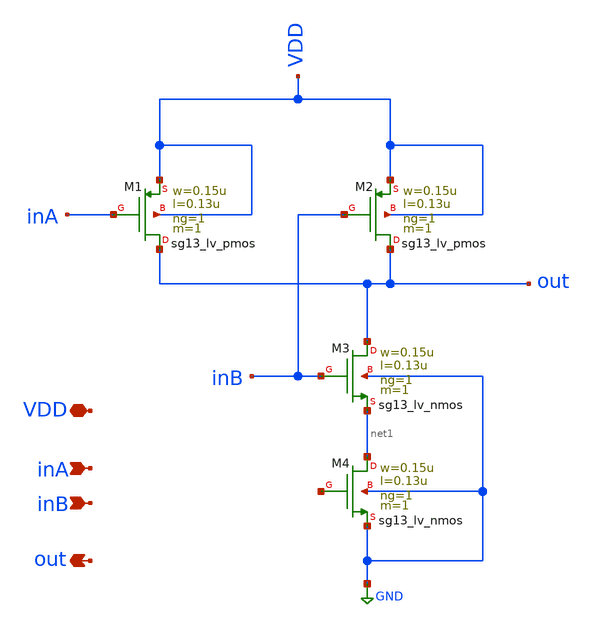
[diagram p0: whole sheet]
** sch_path: Team 2 Design/design_data/xschem/t2_nand2.sch
**.subckt t2_nand2 VDD inA inB out
*.iopin VDD
*.ipin inA
*.ipin inB
*.opin out
XM1 out inA VDD VDD sg13_lv_pmos w=0.15u l=0.13u ng=1 m=1 mm_ok=1
XM2 out inB VDD VDD sg13_lv_pmos w=0.15u l=0.13u ng=1 m=1 mm_ok=1
XM3 out inB net1 GND sg13_lv_nmos w=0.15u l=0.13u ng=1 m=1 mm_ok=1
XM4 net1 net2 GND GND sg13_lv_nmos w=0.15u l=0.13u ng=1 m=1 mm_ok=1
**.ends
.GLOBAL GND
.end
